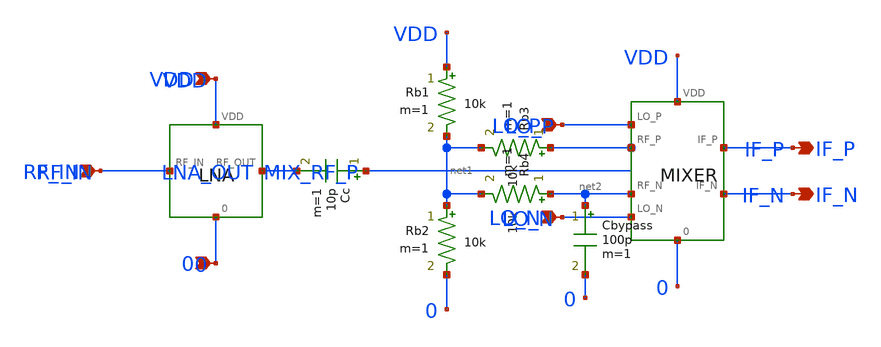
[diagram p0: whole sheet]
** sch_path: modules/PandaChip/designs/rf_trans/rx_top.sch
**.subckt rx_top RF_IN LO_P LO_N IF_P IF_N VDD 0
*.ipin RF_IN
*.ipin LO_P
*.ipin LO_N
*.opin IF_P
*.opin IF_N
*.ipin VDD
*.ipin 0
X1 VDD 0 RF_IN LNA_OUT lna
X2 VDD 0 MIX_RF_P net2 LO_P LO_N IF_P IF_N mixer
Cc MIX_RF_P LNA_OUT 10p m=1
Rb1 VDD net1 10k m=1
Rb2 net1 0 10k m=1
Rb3 MIX_RF_P net1 10k m=1
Rb4 net2 net1 10k m=1
Cbypass net2 0 100p m=1
**.ends

* expanding   symbol:  lna.sym # of pins=4
** sym_path: modules/PandaChip/designs/rf_trans/lna.sym
** sch_path: modules/PandaChip/designs/rf_trans/lna.sch
.subckt lna VDD 0 RF_IN RF_OUT
*.ipin VDD
*.ipin RF_IN
*.opin RF_OUT
*.ipin 0
XM1 MID VBIAS1 0 0 nfet_03v3 L=0.28u W=50u nf=5 ad='int((nf+1)/2) * W/nf * 0.18u' as='int((nf+2)/2) * W/nf * 0.18u'
+ pd='2*int((nf+1)/2) * (W/nf + 0.18u)' ps='2*int((nf+2)/2) * (W/nf + 0.18u)' nrd='0.18u / W' nrs='0.18u / W'
+ sa=0 sb=0 sd=0 m=1
XM2 RF_OUT VBIAS2 MID 0 nfet_03v3 L=0.28u W=50u nf=5 ad='int((nf+1)/2) * W/nf * 0.18u' as='int((nf+2)/2) * W/nf * 0.18u'
+ pd='2*int((nf+1)/2) * (W/nf + 0.18u)' ps='2*int((nf+2)/2) * (W/nf + 0.18u)' nrd='0.18u / W' nrs='0.18u / W'
+ sa=0 sb=0 sd=0 m=1
L1 VDD RF_OUT 100n m=1
C1 VDD RF_OUT 25.3p m=1
R_load VDD RF_OUT 2k m=1
Cin VBIAS1 RF_IN 10p m=1
R1 VDD VBIAS2 15k m=1
R2 VBIAS2 0 18k m=1
R3 VDD VBIAS1 25k m=1
R4 VBIAS1 0 8k m=1
.ends


* expanding   symbol:  mixer.sym # of pins=8
** sym_path: modules/PandaChip/designs/rf_trans/mixer.sym
** sch_path: modules/PandaChip/designs/rf_trans/mixer.sch
.subckt mixer VDD 0 RF_P RF_N LO_P LO_N IF_P IF_N
*.ipin VDD
*.ipin 0
*.ipin RF_P
*.ipin RF_N
*.ipin LO_P
*.ipin LO_N
*.opin IF_P
*.opin IF_N
XM1 M1D RF_P TAIL 0 nfet_03v3 L=0.28u W=50u nf=5 ad='int((nf+1)/2) * W/nf * 0.18u' as='int((nf+2)/2) * W/nf * 0.18u'
+ pd='2*int((nf+1)/2) * (W/nf + 0.18u)' ps='2*int((nf+2)/2) * (W/nf + 0.18u)' nrd='0.18u / W' nrs='0.18u / W'
+ sa=0 sb=0 sd=0 m=1
XM2 M2D RF_N TAIL 0 nfet_03v3 L=0.28u W=50u nf=5 ad='int((nf+1)/2) * W/nf * 0.18u' as='int((nf+2)/2) * W/nf * 0.18u'
+ pd='2*int((nf+1)/2) * (W/nf + 0.18u)' ps='2*int((nf+2)/2) * (W/nf + 0.18u)' nrd='0.18u / W' nrs='0.18u / W'
+ sa=0 sb=0 sd=0 m=1
XM3 IF_P LO_P M1D 0 nfet_03v3 L=0.28u W=50u nf=5 ad='int((nf+1)/2) * W/nf * 0.18u' as='int((nf+2)/2) * W/nf * 0.18u'
+ pd='2*int((nf+1)/2) * (W/nf + 0.18u)' ps='2*int((nf+2)/2) * (W/nf + 0.18u)' nrd='0.18u / W' nrs='0.18u / W'
+ sa=0 sb=0 sd=0 m=1
XM4 IF_N LO_N M1D 0 nfet_03v3 L=0.28u W=50u nf=5 ad='int((nf+1)/2) * W/nf * 0.18u' as='int((nf+2)/2) * W/nf * 0.18u'
+ pd='2*int((nf+1)/2) * (W/nf + 0.18u)' ps='2*int((nf+2)/2) * (W/nf + 0.18u)' nrd='0.18u / W' nrs='0.18u / W'
+ sa=0 sb=0 sd=0 m=1
XM5 IF_P LO_N M2D 0 nfet_03v3 L=0.28u W=50u nf=5 ad='int((nf+1)/2) * W/nf * 0.18u' as='int((nf+2)/2) * W/nf * 0.18u'
+ pd='2*int((nf+1)/2) * (W/nf + 0.18u)' ps='2*int((nf+2)/2) * (W/nf + 0.18u)' nrd='0.18u / W' nrs='0.18u / W'
+ sa=0 sb=0 sd=0 m=1
XM6 IF_N LO_P M2D 0 nfet_03v3 L=0.28u W=50u nf=5 ad='int((nf+1)/2) * W/nf * 0.18u' as='int((nf+2)/2) * W/nf * 0.18u'
+ pd='2*int((nf+1)/2) * (W/nf + 0.18u)' ps='2*int((nf+2)/2) * (W/nf + 0.18u)' nrd='0.18u / W' nrs='0.18u / W'
+ sa=0 sb=0 sd=0 m=1
R1 VDD IF_P 2k m=1
R2 VDD IF_N 2k m=1
I1 TAIL 0 2m
.ends

.end
